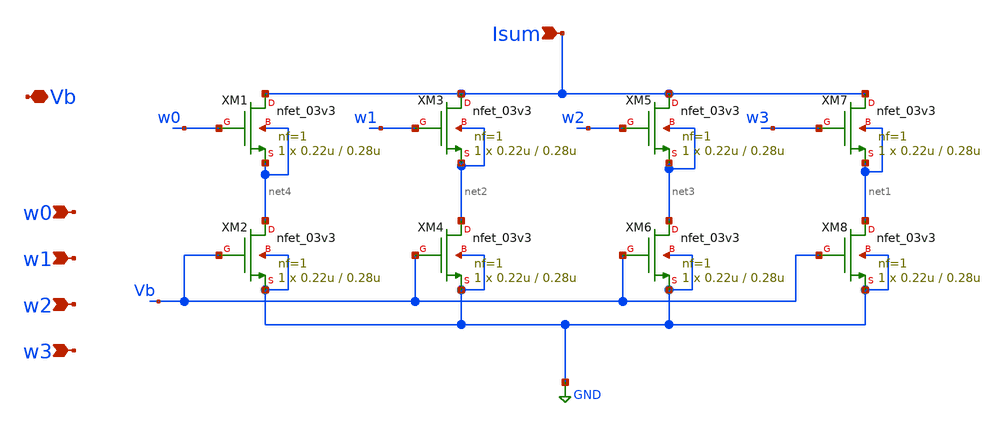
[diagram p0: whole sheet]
** sch_path: analog/neuron/DAC.sch
**.subckt DAC Vb w0 w1 w2 w3 Isum
*.iopin Vb
*.ipin w0
*.ipin w1
*.ipin w2
*.ipin w3
*.ipin Isum
XM1 Isum w0 net4 net4 nfet_03v3 L=0.28u W=0.22u nf=1 ad='int((nf+1)/2) * W/nf * 0.18u' as='int((nf+2)/2) * W/nf * 0.18u'
+ pd='2*int((nf+1)/2) * (W/nf + 0.18u)' ps='2*int((nf+2)/2) * (W/nf + 0.18u)' nrd='0.18u / W' nrs='0.18u / W'
+ sa=0 sb=0 sd=0 m=1
XM2 net4 Vb GND GND nfet_03v3 L=0.28u W=0.22u nf=1 ad='int((nf+1)/2) * W/nf * 0.18u' as='int((nf+2)/2) * W/nf * 0.18u'
+ pd='2*int((nf+1)/2) * (W/nf + 0.18u)' ps='2*int((nf+2)/2) * (W/nf + 0.18u)' nrd='0.18u / W' nrs='0.18u / W'
+ sa=0 sb=0 sd=0 m=1
XM3 Isum w1 net2 net2 nfet_03v3 L=0.28u W=0.22u nf=1 ad='int((nf+1)/2) * W/nf * 0.18u' as='int((nf+2)/2) * W/nf * 0.18u'
+ pd='2*int((nf+1)/2) * (W/nf + 0.18u)' ps='2*int((nf+2)/2) * (W/nf + 0.18u)' nrd='0.18u / W' nrs='0.18u / W'
+ sa=0 sb=0 sd=0 m=1
XM4 net2 Vb GND GND nfet_03v3 L=0.28u W=0.22u nf=1 ad='int((nf+1)/2) * W/nf * 0.18u' as='int((nf+2)/2) * W/nf * 0.18u'
+ pd='2*int((nf+1)/2) * (W/nf + 0.18u)' ps='2*int((nf+2)/2) * (W/nf + 0.18u)' nrd='0.18u / W' nrs='0.18u / W'
+ sa=0 sb=0 sd=0 m=1
XM5 Isum w2 net3 net3 nfet_03v3 L=0.28u W=0.22u nf=1 ad='int((nf+1)/2) * W/nf * 0.18u' as='int((nf+2)/2) * W/nf * 0.18u'
+ pd='2*int((nf+1)/2) * (W/nf + 0.18u)' ps='2*int((nf+2)/2) * (W/nf + 0.18u)' nrd='0.18u / W' nrs='0.18u / W'
+ sa=0 sb=0 sd=0 m=1
XM6 net3 Vb GND GND nfet_03v3 L=0.28u W=0.22u nf=1 ad='int((nf+1)/2) * W/nf * 0.18u' as='int((nf+2)/2) * W/nf * 0.18u'
+ pd='2*int((nf+1)/2) * (W/nf + 0.18u)' ps='2*int((nf+2)/2) * (W/nf + 0.18u)' nrd='0.18u / W' nrs='0.18u / W'
+ sa=0 sb=0 sd=0 m=1
XM7 Isum w3 net1 net1 nfet_03v3 L=0.28u W=0.22u nf=1 ad='int((nf+1)/2) * W/nf * 0.18u' as='int((nf+2)/2) * W/nf * 0.18u'
+ pd='2*int((nf+1)/2) * (W/nf + 0.18u)' ps='2*int((nf+2)/2) * (W/nf + 0.18u)' nrd='0.18u / W' nrs='0.18u / W'
+ sa=0 sb=0 sd=0 m=1
XM8 net1 Vb GND GND nfet_03v3 L=0.28u W=0.22u nf=1 ad='int((nf+1)/2) * W/nf * 0.18u' as='int((nf+2)/2) * W/nf * 0.18u'
+ pd='2*int((nf+1)/2) * (W/nf + 0.18u)' ps='2*int((nf+2)/2) * (W/nf + 0.18u)' nrd='0.18u / W' nrs='0.18u / W'
+ sa=0 sb=0 sd=0 m=1
**.ends
.GLOBAL GND
.end
